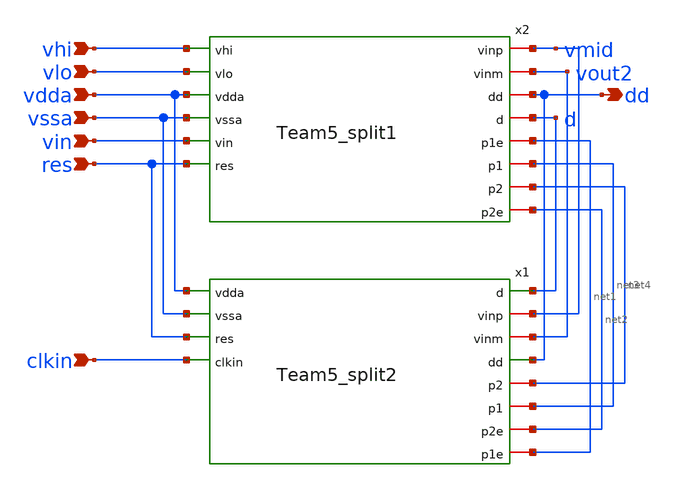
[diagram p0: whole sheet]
** sch_path: 5_Design/4_Layout/Team 5/Team5.sch
**.subckt Team5 vhi vlo vdda vssa vin res dd clkin
*.ipin vhi
*.ipin vlo
*.ipin vdda
*.ipin vssa
*.ipin vin
*.ipin res
*.opin dd
*.ipin clkin
x2 vhi vlo vdda vssa vmid vin vout2 dd d res net1 net3 net4 net2 Team5_split1
x1 vdda vssa d vmid vout2 dd res net4 net3 net2 net1 clkin Team5_split2
**.ends
.end
